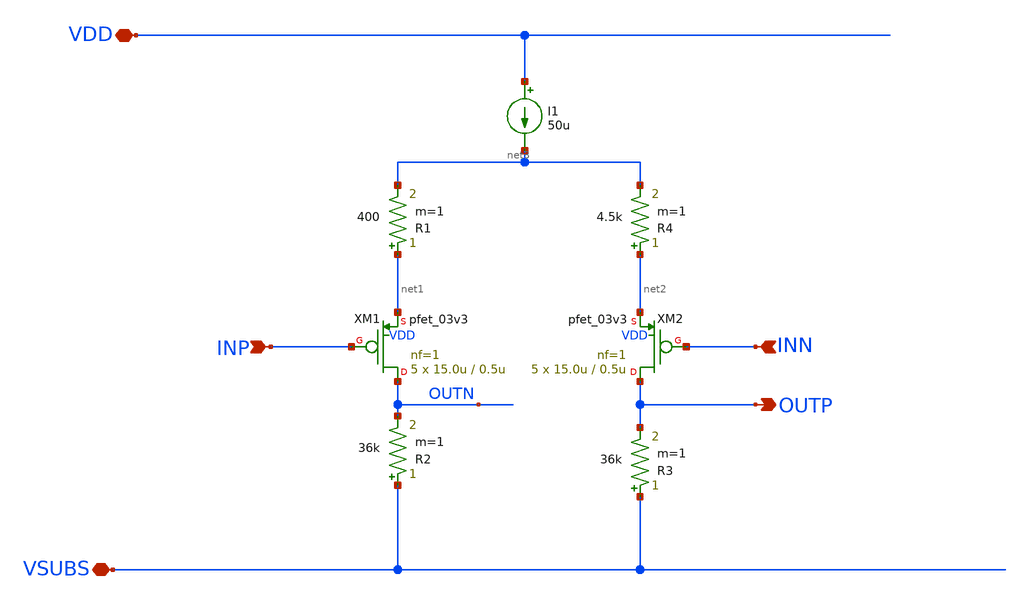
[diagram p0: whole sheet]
** sch_path: xschem/ip_amplifier.sch
**.subckt ip_amplifier VDD VSUBS INP INN OUTP
*.iopin VDD
*.iopin VSUBS
*.ipin INP
*.ipin INN
*.opin OUTP
XM1 OUTN INP net1 VDD pfet_03v3 L=0.5u W=15.0u nf=1 ad='int((nf+1)/2) * W/nf * 0.18u' as='int((nf+2)/2) * W/nf * 0.18u'
+ pd='2*int((nf+1)/2) * (W/nf + 0.18u)' ps='2*int((nf+2)/2) * (W/nf + 0.18u)' nrd='0.18u / W' nrs='0.18u / W'
+ sa=0 sb=0 sd=0 m=5 par=5
XM2 OUTP INN net2 VDD pfet_03v3 L=0.5u W=15.0u nf=1 ad='int((nf+1)/2) * W/nf * 0.18u' as='int((nf+2)/2) * W/nf * 0.18u'
+ pd='2*int((nf+1)/2) * (W/nf + 0.18u)' ps='2*int((nf+2)/2) * (W/nf + 0.18u)' nrd='0.18u / W' nrs='0.18u / W'
+ sa=0 sb=0 sd=0 m=5 par=5
R2 VSUBS OUTN 36k m=1
R3 VSUBS OUTP 36k m=1
I1 VDD net3 50u
R4 net2 net3 4.5k m=1
R1 net1 net3 400 m=1
**.ends
.end
